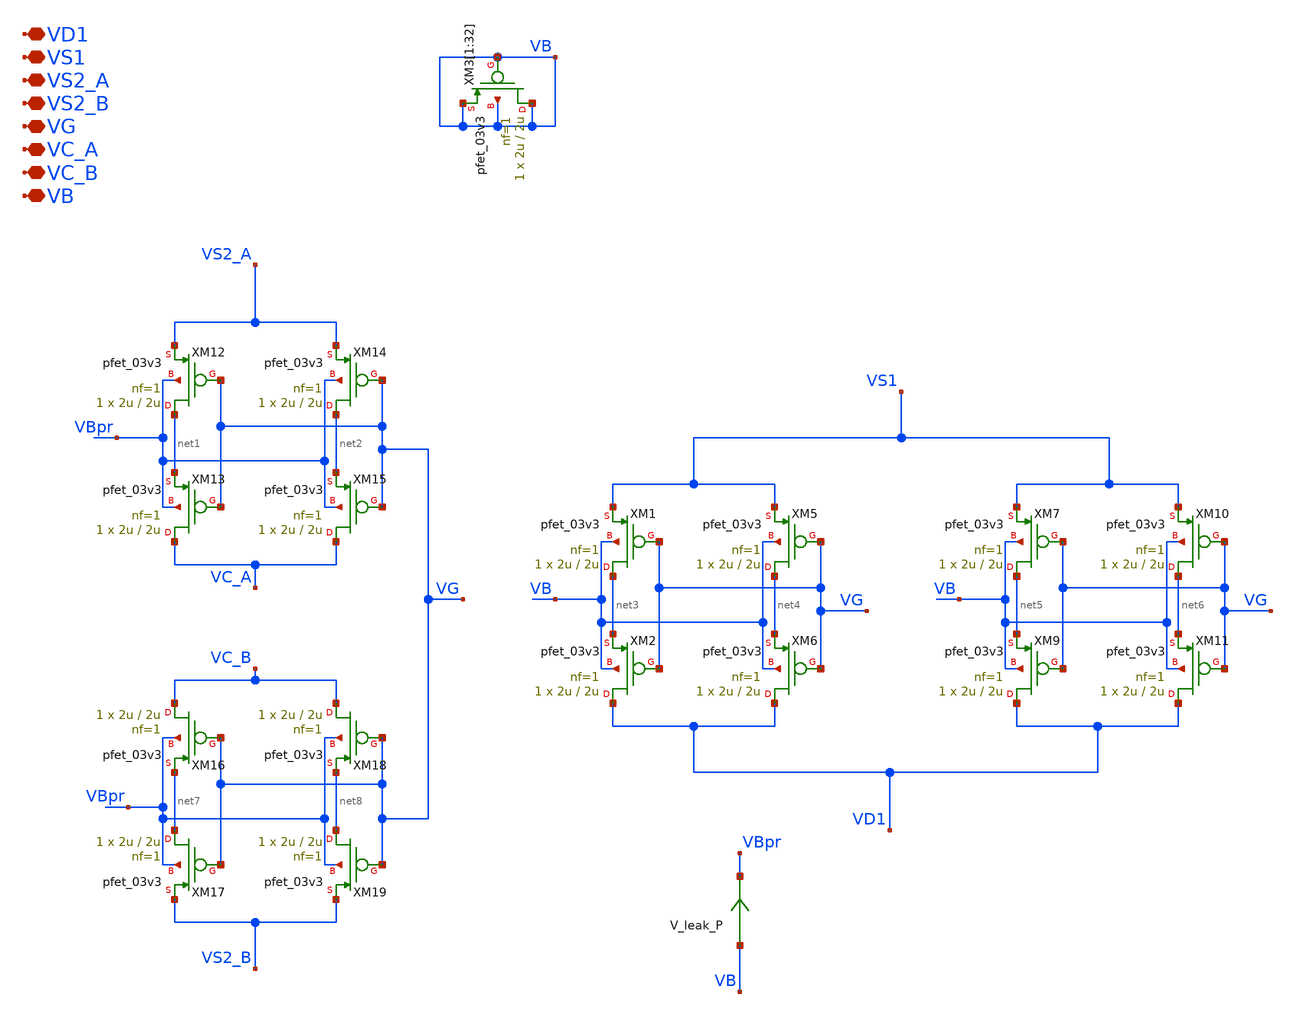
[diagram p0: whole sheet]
** sch_path: TIA_Filter/PseudoResistor/PR_pfets.sch
**.subckt PR_pfets VD1 VS1 VS2_A VS2_B VG VC_A VC_B VB
*.iopin VD1
*.iopin VS1
*.iopin VS2_A
*.iopin VS2_B
*.iopin VG
*.iopin VC_A
*.iopin VC_B
*.iopin VB
XM1 net3 VG VS1 VB pfet_03v3 L=2u W=2u nf=1 ad='int((nf+1)/2) * W/nf * 0.18u' as='int((nf+2)/2) * W/nf * 0.18u'
+ pd='2*int((nf+1)/2) * (W/nf + 0.18u)' ps='2*int((nf+2)/2) * (W/nf + 0.18u)' nrd='0.18u / W' nrs='0.18u / W'
+ sa=0 sb=0 sd=0 m=1
XM2 VD1 VG net3 VB pfet_03v3 L=2u W=2u nf=1 ad='int((nf+1)/2) * W/nf * 0.18u' as='int((nf+2)/2) * W/nf * 0.18u'
+ pd='2*int((nf+1)/2) * (W/nf + 0.18u)' ps='2*int((nf+2)/2) * (W/nf + 0.18u)' nrd='0.18u / W' nrs='0.18u / W'
+ sa=0 sb=0 sd=0 m=1
XM5 net4 VG VS1 VB pfet_03v3 L=2u W=2u nf=1 ad='int((nf+1)/2) * W/nf * 0.18u' as='int((nf+2)/2) * W/nf * 0.18u'
+ pd='2*int((nf+1)/2) * (W/nf + 0.18u)' ps='2*int((nf+2)/2) * (W/nf + 0.18u)' nrd='0.18u / W' nrs='0.18u / W'
+ sa=0 sb=0 sd=0 m=1
XM6 VD1 VG net4 VB pfet_03v3 L=2u W=2u nf=1 ad='int((nf+1)/2) * W/nf * 0.18u' as='int((nf+2)/2) * W/nf * 0.18u'
+ pd='2*int((nf+1)/2) * (W/nf + 0.18u)' ps='2*int((nf+2)/2) * (W/nf + 0.18u)' nrd='0.18u / W' nrs='0.18u / W'
+ sa=0 sb=0 sd=0 m=1
XM7 net5 VG VS1 VB pfet_03v3 L=2u W=2u nf=1 ad='int((nf+1)/2) * W/nf * 0.18u' as='int((nf+2)/2) * W/nf * 0.18u'
+ pd='2*int((nf+1)/2) * (W/nf + 0.18u)' ps='2*int((nf+2)/2) * (W/nf + 0.18u)' nrd='0.18u / W' nrs='0.18u / W'
+ sa=0 sb=0 sd=0 m=1
XM9 VD1 VG net5 VB pfet_03v3 L=2u W=2u nf=1 ad='int((nf+1)/2) * W/nf * 0.18u' as='int((nf+2)/2) * W/nf * 0.18u'
+ pd='2*int((nf+1)/2) * (W/nf + 0.18u)' ps='2*int((nf+2)/2) * (W/nf + 0.18u)' nrd='0.18u / W' nrs='0.18u / W'
+ sa=0 sb=0 sd=0 m=1
XM10 net6 VG VS1 VB pfet_03v3 L=2u W=2u nf=1 ad='int((nf+1)/2) * W/nf * 0.18u' as='int((nf+2)/2) * W/nf * 0.18u'
+ pd='2*int((nf+1)/2) * (W/nf + 0.18u)' ps='2*int((nf+2)/2) * (W/nf + 0.18u)' nrd='0.18u / W' nrs='0.18u / W'
+ sa=0 sb=0 sd=0 m=1
XM11 VD1 VG net6 VB pfet_03v3 L=2u W=2u nf=1 ad='int((nf+1)/2) * W/nf * 0.18u' as='int((nf+2)/2) * W/nf * 0.18u'
+ pd='2*int((nf+1)/2) * (W/nf + 0.18u)' ps='2*int((nf+2)/2) * (W/nf + 0.18u)' nrd='0.18u / W' nrs='0.18u / W'
+ sa=0 sb=0 sd=0 m=1
XM12 net1 VG VS2_A VBpr pfet_03v3 L=2u W=2u nf=1 ad='int((nf+1)/2) * W/nf * 0.18u' as='int((nf+2)/2) * W/nf * 0.18u'
+ pd='2*int((nf+1)/2) * (W/nf + 0.18u)' ps='2*int((nf+2)/2) * (W/nf + 0.18u)' nrd='0.18u / W' nrs='0.18u / W'
+ sa=0 sb=0 sd=0 m=1
XM13 VC_A VG net1 VBpr pfet_03v3 L=2u W=2u nf=1 ad='int((nf+1)/2) * W/nf * 0.18u' as='int((nf+2)/2) * W/nf * 0.18u'
+ pd='2*int((nf+1)/2) * (W/nf + 0.18u)' ps='2*int((nf+2)/2) * (W/nf + 0.18u)' nrd='0.18u / W' nrs='0.18u / W'
+ sa=0 sb=0 sd=0 m=1
XM14 net2 VG VS2_A VBpr pfet_03v3 L=2u W=2u nf=1 ad='int((nf+1)/2) * W/nf * 0.18u' as='int((nf+2)/2) * W/nf * 0.18u'
+ pd='2*int((nf+1)/2) * (W/nf + 0.18u)' ps='2*int((nf+2)/2) * (W/nf + 0.18u)' nrd='0.18u / W' nrs='0.18u / W'
+ sa=0 sb=0 sd=0 m=1
XM15 VC_A VG net2 VBpr pfet_03v3 L=2u W=2u nf=1 ad='int((nf+1)/2) * W/nf * 0.18u' as='int((nf+2)/2) * W/nf * 0.18u'
+ pd='2*int((nf+1)/2) * (W/nf + 0.18u)' ps='2*int((nf+2)/2) * (W/nf + 0.18u)' nrd='0.18u / W' nrs='0.18u / W'
+ sa=0 sb=0 sd=0 m=1
XM16 VC_B VG net7 VBpr pfet_03v3 L=2u W=2u nf=1 ad='int((nf+1)/2) * W/nf * 0.18u' as='int((nf+2)/2) * W/nf * 0.18u'
+ pd='2*int((nf+1)/2) * (W/nf + 0.18u)' ps='2*int((nf+2)/2) * (W/nf + 0.18u)' nrd='0.18u / W' nrs='0.18u / W'
+ sa=0 sb=0 sd=0 m=1
XM17 net7 VG VS2_B VBpr pfet_03v3 L=2u W=2u nf=1 ad='int((nf+1)/2) * W/nf * 0.18u' as='int((nf+2)/2) * W/nf * 0.18u'
+ pd='2*int((nf+1)/2) * (W/nf + 0.18u)' ps='2*int((nf+2)/2) * (W/nf + 0.18u)' nrd='0.18u / W' nrs='0.18u / W'
+ sa=0 sb=0 sd=0 m=1
XM18 VC_B VG net8 VBpr pfet_03v3 L=2u W=2u nf=1 ad='int((nf+1)/2) * W/nf * 0.18u' as='int((nf+2)/2) * W/nf * 0.18u'
+ pd='2*int((nf+1)/2) * (W/nf + 0.18u)' ps='2*int((nf+2)/2) * (W/nf + 0.18u)' nrd='0.18u / W' nrs='0.18u / W'
+ sa=0 sb=0 sd=0 m=1
XM19 net8 VG VS2_B VBpr pfet_03v3 L=2u W=2u nf=1 ad='int((nf+1)/2) * W/nf * 0.18u' as='int((nf+2)/2) * W/nf * 0.18u'
+ pd='2*int((nf+1)/2) * (W/nf + 0.18u)' ps='2*int((nf+2)/2) * (W/nf + 0.18u)' nrd='0.18u / W' nrs='0.18u / W'
+ sa=0 sb=0 sd=0 m=1
XM3[1] VB VB VB VB pfet_03v3 L=2u W=2u nf=1 ad='int((nf+1)/2) * W/nf * 0.18u' as='int((nf+2)/2) * W/nf * 0.18u'
+ pd='2*int((nf+1)/2) * (W/nf + 0.18u)' ps='2*int((nf+2)/2) * (W/nf + 0.18u)' nrd='0.18u / W' nrs='0.18u / W'
+ sa=0 sb=0 sd=0 m=1
XM3[2] VB VB VB VB pfet_03v3 L=2u W=2u nf=1 ad='int((nf+1)/2) * W/nf * 0.18u' as='int((nf+2)/2) * W/nf * 0.18u'
+ pd='2*int((nf+1)/2) * (W/nf + 0.18u)' ps='2*int((nf+2)/2) * (W/nf + 0.18u)' nrd='0.18u / W' nrs='0.18u / W'
+ sa=0 sb=0 sd=0 m=1
XM3[3] VB VB VB VB pfet_03v3 L=2u W=2u nf=1 ad='int((nf+1)/2) * W/nf * 0.18u' as='int((nf+2)/2) * W/nf * 0.18u'
+ pd='2*int((nf+1)/2) * (W/nf + 0.18u)' ps='2*int((nf+2)/2) * (W/nf + 0.18u)' nrd='0.18u / W' nrs='0.18u / W'
+ sa=0 sb=0 sd=0 m=1
XM3[4] VB VB VB VB pfet_03v3 L=2u W=2u nf=1 ad='int((nf+1)/2) * W/nf * 0.18u' as='int((nf+2)/2) * W/nf * 0.18u'
+ pd='2*int((nf+1)/2) * (W/nf + 0.18u)' ps='2*int((nf+2)/2) * (W/nf + 0.18u)' nrd='0.18u / W' nrs='0.18u / W'
+ sa=0 sb=0 sd=0 m=1
XM3[5] VB VB VB VB pfet_03v3 L=2u W=2u nf=1 ad='int((nf+1)/2) * W/nf * 0.18u' as='int((nf+2)/2) * W/nf * 0.18u'
+ pd='2*int((nf+1)/2) * (W/nf + 0.18u)' ps='2*int((nf+2)/2) * (W/nf + 0.18u)' nrd='0.18u / W' nrs='0.18u / W'
+ sa=0 sb=0 sd=0 m=1
XM3[6] VB VB VB VB pfet_03v3 L=2u W=2u nf=1 ad='int((nf+1)/2) * W/nf * 0.18u' as='int((nf+2)/2) * W/nf * 0.18u'
+ pd='2*int((nf+1)/2) * (W/nf + 0.18u)' ps='2*int((nf+2)/2) * (W/nf + 0.18u)' nrd='0.18u / W' nrs='0.18u / W'
+ sa=0 sb=0 sd=0 m=1
XM3[7] VB VB VB VB pfet_03v3 L=2u W=2u nf=1 ad='int((nf+1)/2) * W/nf * 0.18u' as='int((nf+2)/2) * W/nf * 0.18u'
+ pd='2*int((nf+1)/2) * (W/nf + 0.18u)' ps='2*int((nf+2)/2) * (W/nf + 0.18u)' nrd='0.18u / W' nrs='0.18u / W'
+ sa=0 sb=0 sd=0 m=1
XM3[8] VB VB VB VB pfet_03v3 L=2u W=2u nf=1 ad='int((nf+1)/2) * W/nf * 0.18u' as='int((nf+2)/2) * W/nf * 0.18u'
+ pd='2*int((nf+1)/2) * (W/nf + 0.18u)' ps='2*int((nf+2)/2) * (W/nf + 0.18u)' nrd='0.18u / W' nrs='0.18u / W'
+ sa=0 sb=0 sd=0 m=1
XM3[9] VB VB VB VB pfet_03v3 L=2u W=2u nf=1 ad='int((nf+1)/2) * W/nf * 0.18u' as='int((nf+2)/2) * W/nf * 0.18u'
+ pd='2*int((nf+1)/2) * (W/nf + 0.18u)' ps='2*int((nf+2)/2) * (W/nf + 0.18u)' nrd='0.18u / W' nrs='0.18u / W'
+ sa=0 sb=0 sd=0 m=1
XM3[10] VB VB VB VB pfet_03v3 L=2u W=2u nf=1 ad='int((nf+1)/2) * W/nf * 0.18u' as='int((nf+2)/2) * W/nf * 0.18u'
+ pd='2*int((nf+1)/2) * (W/nf + 0.18u)' ps='2*int((nf+2)/2) * (W/nf + 0.18u)' nrd='0.18u / W' nrs='0.18u / W'
+ sa=0 sb=0 sd=0 m=1
XM3[11] VB VB VB VB pfet_03v3 L=2u W=2u nf=1 ad='int((nf+1)/2) * W/nf * 0.18u' as='int((nf+2)/2) * W/nf * 0.18u'
+ pd='2*int((nf+1)/2) * (W/nf + 0.18u)' ps='2*int((nf+2)/2) * (W/nf + 0.18u)' nrd='0.18u / W' nrs='0.18u / W'
+ sa=0 sb=0 sd=0 m=1
XM3[12] VB VB VB VB pfet_03v3 L=2u W=2u nf=1 ad='int((nf+1)/2) * W/nf * 0.18u' as='int((nf+2)/2) * W/nf * 0.18u'
+ pd='2*int((nf+1)/2) * (W/nf + 0.18u)' ps='2*int((nf+2)/2) * (W/nf + 0.18u)' nrd='0.18u / W' nrs='0.18u / W'
+ sa=0 sb=0 sd=0 m=1
XM3[13] VB VB VB VB pfet_03v3 L=2u W=2u nf=1 ad='int((nf+1)/2) * W/nf * 0.18u' as='int((nf+2)/2) * W/nf * 0.18u'
+ pd='2*int((nf+1)/2) * (W/nf + 0.18u)' ps='2*int((nf+2)/2) * (W/nf + 0.18u)' nrd='0.18u / W' nrs='0.18u / W'
+ sa=0 sb=0 sd=0 m=1
XM3[14] VB VB VB VB pfet_03v3 L=2u W=2u nf=1 ad='int((nf+1)/2) * W/nf * 0.18u' as='int((nf+2)/2) * W/nf * 0.18u'
+ pd='2*int((nf+1)/2) * (W/nf + 0.18u)' ps='2*int((nf+2)/2) * (W/nf + 0.18u)' nrd='0.18u / W' nrs='0.18u / W'
+ sa=0 sb=0 sd=0 m=1
XM3[15] VB VB VB VB pfet_03v3 L=2u W=2u nf=1 ad='int((nf+1)/2) * W/nf * 0.18u' as='int((nf+2)/2) * W/nf * 0.18u'
+ pd='2*int((nf+1)/2) * (W/nf + 0.18u)' ps='2*int((nf+2)/2) * (W/nf + 0.18u)' nrd='0.18u / W' nrs='0.18u / W'
+ sa=0 sb=0 sd=0 m=1
XM3[16] VB VB VB VB pfet_03v3 L=2u W=2u nf=1 ad='int((nf+1)/2) * W/nf * 0.18u' as='int((nf+2)/2) * W/nf * 0.18u'
+ pd='2*int((nf+1)/2) * (W/nf + 0.18u)' ps='2*int((nf+2)/2) * (W/nf + 0.18u)' nrd='0.18u / W' nrs='0.18u / W'
+ sa=0 sb=0 sd=0 m=1
XM3[17] VB VB VB VB pfet_03v3 L=2u W=2u nf=1 ad='int((nf+1)/2) * W/nf * 0.18u' as='int((nf+2)/2) * W/nf * 0.18u'
+ pd='2*int((nf+1)/2) * (W/nf + 0.18u)' ps='2*int((nf+2)/2) * (W/nf + 0.18u)' nrd='0.18u / W' nrs='0.18u / W'
+ sa=0 sb=0 sd=0 m=1
XM3[18] VB VB VB VB pfet_03v3 L=2u W=2u nf=1 ad='int((nf+1)/2) * W/nf * 0.18u' as='int((nf+2)/2) * W/nf * 0.18u'
+ pd='2*int((nf+1)/2) * (W/nf + 0.18u)' ps='2*int((nf+2)/2) * (W/nf + 0.18u)' nrd='0.18u / W' nrs='0.18u / W'
+ sa=0 sb=0 sd=0 m=1
XM3[19] VB VB VB VB pfet_03v3 L=2u W=2u nf=1 ad='int((nf+1)/2) * W/nf * 0.18u' as='int((nf+2)/2) * W/nf * 0.18u'
+ pd='2*int((nf+1)/2) * (W/nf + 0.18u)' ps='2*int((nf+2)/2) * (W/nf + 0.18u)' nrd='0.18u / W' nrs='0.18u / W'
+ sa=0 sb=0 sd=0 m=1
XM3[20] VB VB VB VB pfet_03v3 L=2u W=2u nf=1 ad='int((nf+1)/2) * W/nf * 0.18u' as='int((nf+2)/2) * W/nf * 0.18u'
+ pd='2*int((nf+1)/2) * (W/nf + 0.18u)' ps='2*int((nf+2)/2) * (W/nf + 0.18u)' nrd='0.18u / W' nrs='0.18u / W'
+ sa=0 sb=0 sd=0 m=1
XM3[21] VB VB VB VB pfet_03v3 L=2u W=2u nf=1 ad='int((nf+1)/2) * W/nf * 0.18u' as='int((nf+2)/2) * W/nf * 0.18u'
+ pd='2*int((nf+1)/2) * (W/nf + 0.18u)' ps='2*int((nf+2)/2) * (W/nf + 0.18u)' nrd='0.18u / W' nrs='0.18u / W'
+ sa=0 sb=0 sd=0 m=1
XM3[22] VB VB VB VB pfet_03v3 L=2u W=2u nf=1 ad='int((nf+1)/2) * W/nf * 0.18u' as='int((nf+2)/2) * W/nf * 0.18u'
+ pd='2*int((nf+1)/2) * (W/nf + 0.18u)' ps='2*int((nf+2)/2) * (W/nf + 0.18u)' nrd='0.18u / W' nrs='0.18u / W'
+ sa=0 sb=0 sd=0 m=1
XM3[23] VB VB VB VB pfet_03v3 L=2u W=2u nf=1 ad='int((nf+1)/2) * W/nf * 0.18u' as='int((nf+2)/2) * W/nf * 0.18u'
+ pd='2*int((nf+1)/2) * (W/nf + 0.18u)' ps='2*int((nf+2)/2) * (W/nf + 0.18u)' nrd='0.18u / W' nrs='0.18u / W'
+ sa=0 sb=0 sd=0 m=1
XM3[24] VB VB VB VB pfet_03v3 L=2u W=2u nf=1 ad='int((nf+1)/2) * W/nf * 0.18u' as='int((nf+2)/2) * W/nf * 0.18u'
+ pd='2*int((nf+1)/2) * (W/nf + 0.18u)' ps='2*int((nf+2)/2) * (W/nf + 0.18u)' nrd='0.18u / W' nrs='0.18u / W'
+ sa=0 sb=0 sd=0 m=1
XM3[25] VB VB VB VB pfet_03v3 L=2u W=2u nf=1 ad='int((nf+1)/2) * W/nf * 0.18u' as='int((nf+2)/2) * W/nf * 0.18u'
+ pd='2*int((nf+1)/2) * (W/nf + 0.18u)' ps='2*int((nf+2)/2) * (W/nf + 0.18u)' nrd='0.18u / W' nrs='0.18u / W'
+ sa=0 sb=0 sd=0 m=1
XM3[26] VB VB VB VB pfet_03v3 L=2u W=2u nf=1 ad='int((nf+1)/2) * W/nf * 0.18u' as='int((nf+2)/2) * W/nf * 0.18u'
+ pd='2*int((nf+1)/2) * (W/nf + 0.18u)' ps='2*int((nf+2)/2) * (W/nf + 0.18u)' nrd='0.18u / W' nrs='0.18u / W'
+ sa=0 sb=0 sd=0 m=1
XM3[27] VB VB VB VB pfet_03v3 L=2u W=2u nf=1 ad='int((nf+1)/2) * W/nf * 0.18u' as='int((nf+2)/2) * W/nf * 0.18u'
+ pd='2*int((nf+1)/2) * (W/nf + 0.18u)' ps='2*int((nf+2)/2) * (W/nf + 0.18u)' nrd='0.18u / W' nrs='0.18u / W'
+ sa=0 sb=0 sd=0 m=1
XM3[28] VB VB VB VB pfet_03v3 L=2u W=2u nf=1 ad='int((nf+1)/2) * W/nf * 0.18u' as='int((nf+2)/2) * W/nf * 0.18u'
+ pd='2*int((nf+1)/2) * (W/nf + 0.18u)' ps='2*int((nf+2)/2) * (W/nf + 0.18u)' nrd='0.18u / W' nrs='0.18u / W'
+ sa=0 sb=0 sd=0 m=1
XM3[29] VB VB VB VB pfet_03v3 L=2u W=2u nf=1 ad='int((nf+1)/2) * W/nf * 0.18u' as='int((nf+2)/2) * W/nf * 0.18u'
+ pd='2*int((nf+1)/2) * (W/nf + 0.18u)' ps='2*int((nf+2)/2) * (W/nf + 0.18u)' nrd='0.18u / W' nrs='0.18u / W'
+ sa=0 sb=0 sd=0 m=1
XM3[30] VB VB VB VB pfet_03v3 L=2u W=2u nf=1 ad='int((nf+1)/2) * W/nf * 0.18u' as='int((nf+2)/2) * W/nf * 0.18u'
+ pd='2*int((nf+1)/2) * (W/nf + 0.18u)' ps='2*int((nf+2)/2) * (W/nf + 0.18u)' nrd='0.18u / W' nrs='0.18u / W'
+ sa=0 sb=0 sd=0 m=1
XM3[31] VB VB VB VB pfet_03v3 L=2u W=2u nf=1 ad='int((nf+1)/2) * W/nf * 0.18u' as='int((nf+2)/2) * W/nf * 0.18u'
+ pd='2*int((nf+1)/2) * (W/nf + 0.18u)' ps='2*int((nf+2)/2) * (W/nf + 0.18u)' nrd='0.18u / W' nrs='0.18u / W'
+ sa=0 sb=0 sd=0 m=1
XM3[32] VB VB VB VB pfet_03v3 L=2u W=2u nf=1 ad='int((nf+1)/2) * W/nf * 0.18u' as='int((nf+2)/2) * W/nf * 0.18u'
+ pd='2*int((nf+1)/2) * (W/nf + 0.18u)' ps='2*int((nf+2)/2) * (W/nf + 0.18u)' nrd='0.18u / W' nrs='0.18u / W'
+ sa=0 sb=0 sd=0 m=1
V_leak_P VB VBpr 0
.save i(v_leak_p)
**.ends
.end
